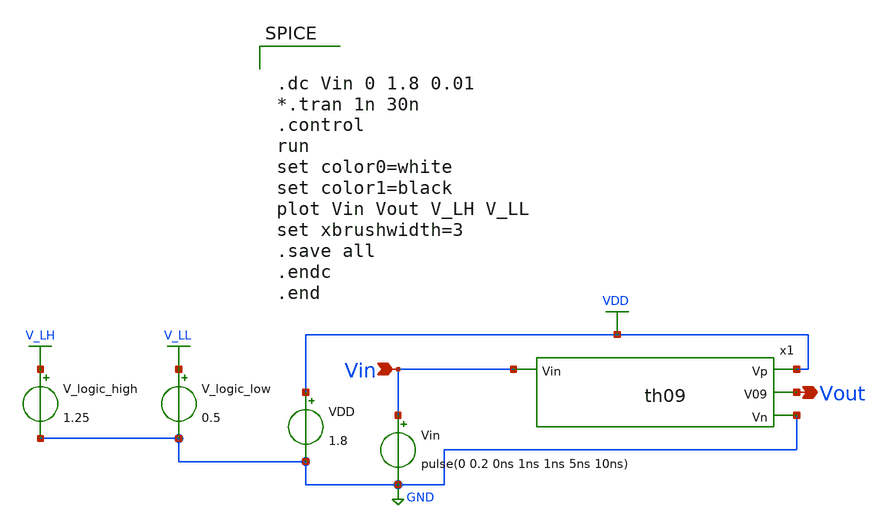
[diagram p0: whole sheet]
** sch_path: xschem/Vth_sch/Pre_layout/th09.sch
**.subckt th09 Vin Vout
*.ipin Vin
*.opin Vout
VDD VDD GND 1.8
Vin Vin GND pulse(0 0.2 0ns 1ns 1ns 5ns 10ns)
V_logic_high V_LH GND 1.25
V_logic_low V_LL GND 0.5
x1 VDD Vout Vin GND th09
**** begin user architecture code


.lib /usr/local/share/pdk/sky130A/libs.tech/ngspice/sky130.lib.spice tt

.save all





.dc Vin 0 1.8 0.01
*.tran 1n 30n
.control
run
set color0=white
set color1=black
plot Vin Vout V_LH V_LL
set xbrushwidth=3
.save all
.endc
.end


**** end user architecture code
**.ends

* expanding   symbol:  /home/exotic/Desktop/ASIC_ADC/xschem/Vth_sch/Symbol/th09.sym # of pins=4
** sym_path: xschem/Vth_sch/Symbol/th09.sym
** sch_path: xschem/Vth_sch/Symbol/th09.sch
.subckt th09 Vp V09 Vin Vn
*.ipin Vin
*.opin V09
*.opin Vn
*.opin Vp
XM2 net2 net1 Vp Vp sky130_fd_pr__pfet_01v8 L=1.57 W=0.42 nf=1 ad='int((nf+1)/2) * W/nf * 0.29' as='int((nf+2)/2) * W/nf * 0.29'
+ pd='2*int((nf+1)/2) * (W/nf + 0.29)' ps='2*int((nf+2)/2) * (W/nf + 0.29)' nrd='0.29 / W' nrs='0.29 / W'
+ sa=0 sb=0 sd=0 mult=1 m=1
XM3 V09 net1 net2 Vp sky130_fd_pr__pfet_01v8 L=1.57 W=0.42 nf=1 ad='int((nf+1)/2) * W/nf * 0.29' as='int((nf+2)/2) * W/nf * 0.29'
+ pd='2*int((nf+1)/2) * (W/nf + 0.29)' ps='2*int((nf+2)/2) * (W/nf + 0.29)' nrd='0.29 / W' nrs='0.29 / W'
+ sa=0 sb=0 sd=0 mult=1 m=1
XM4 V09 net1 Vn Vn sky130_fd_pr__nfet_01v8 L=0.15 W=1.57 nf=1 ad='int((nf+1)/2) * W/nf * 0.29' as='int((nf+2)/2) * W/nf * 0.29'
+ pd='2*int((nf+1)/2) * (W/nf + 0.29)' ps='2*int((nf+2)/2) * (W/nf + 0.29)' nrd='0.29 / W' nrs='0.29 / W'
+ sa=0 sb=0 sd=0 mult=1 m=1
XM1 net1 Vin Vp Vp sky130_fd_pr__pfet_01v8 L=0.15 W=1.58 nf=1 ad='int((nf+1)/2) * W/nf * 0.29' as='int((nf+2)/2) * W/nf * 0.29'
+ pd='2*int((nf+1)/2) * (W/nf + 0.29)' ps='2*int((nf+2)/2) * (W/nf + 0.29)' nrd='0.29 / W' nrs='0.29 / W'
+ sa=0 sb=0 sd=0 mult=1 m=1
XM0 net1 Vin Vn Vn sky130_fd_pr__nfet_01v8 L=1.57 W=0.36 nf=1 ad='int((nf+1)/2) * W/nf * 0.29' as='int((nf+2)/2) * W/nf * 0.29'
+ pd='2*int((nf+1)/2) * (W/nf + 0.29)' ps='2*int((nf+2)/2) * (W/nf + 0.29)' nrd='0.29 / W' nrs='0.29 / W'
+ sa=0 sb=0 sd=0 mult=1 m=1
.ends

.GLOBAL VDD
.GLOBAL GND
.GLOBAL V_LH
.GLOBAL V_LL
.end
